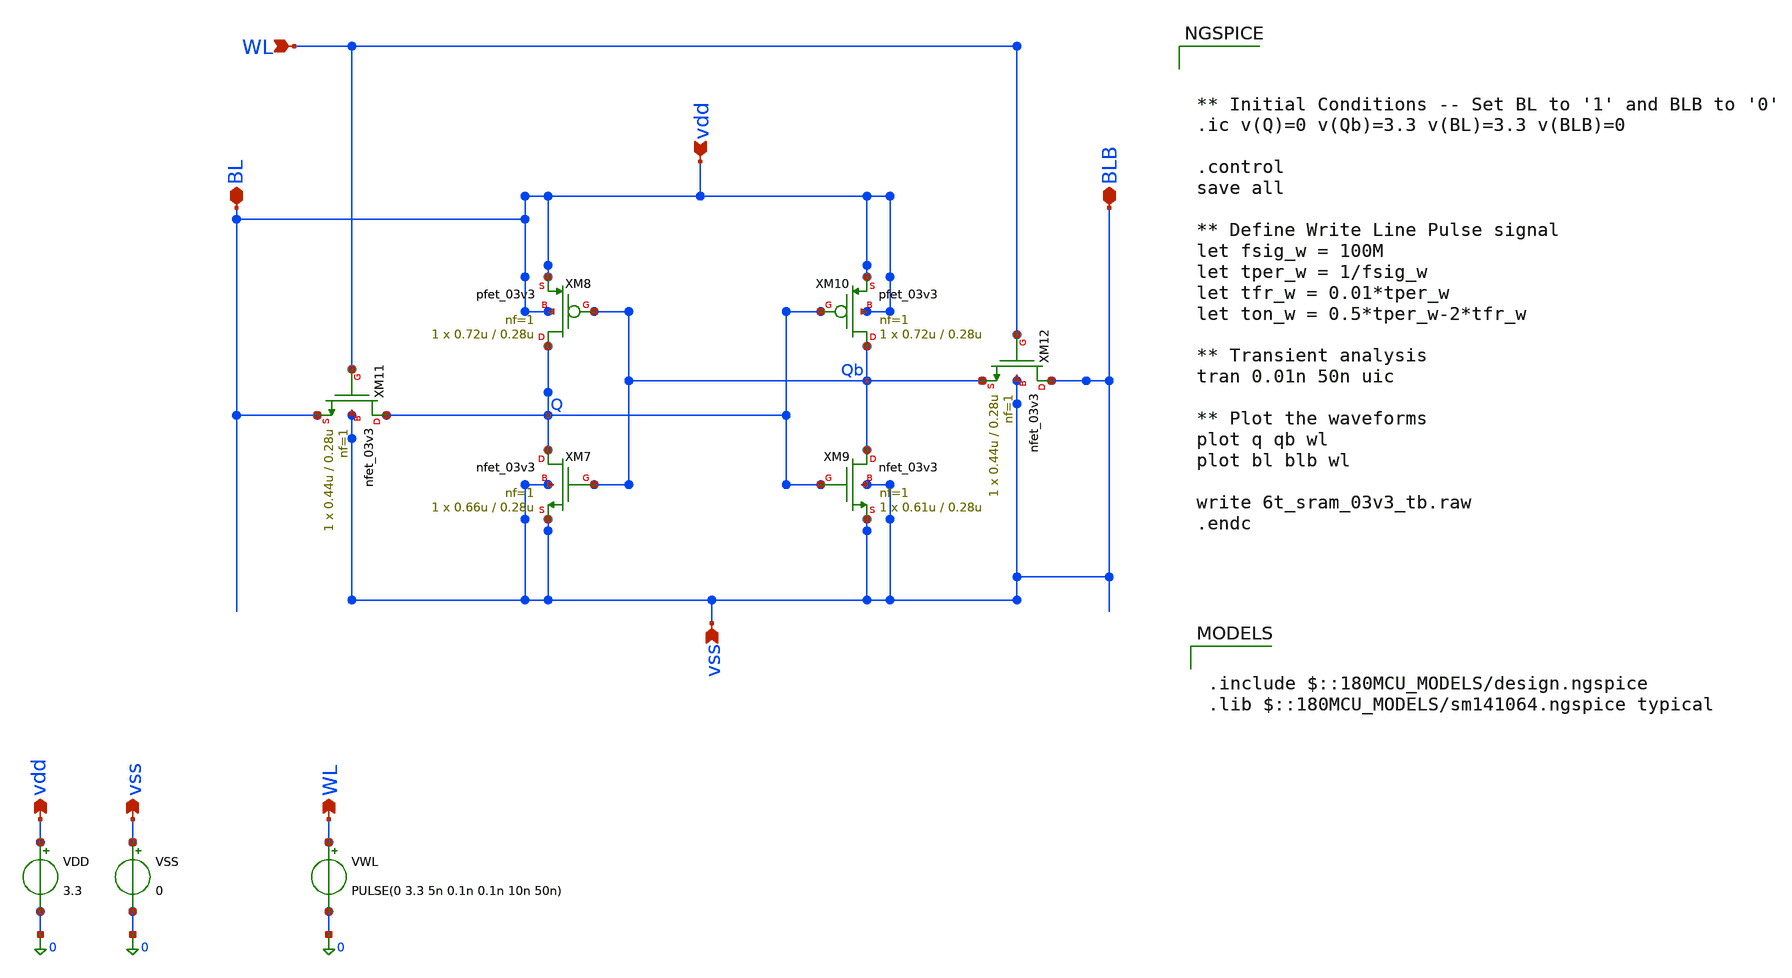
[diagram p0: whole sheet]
** sch_path: analog/designs/6t_sram_03v3_trial.sch
**.subckt 6t_sram_03v3_trial vdd vss WL vdd vss BL WL BLB vdd vss WL vdd vss BL WL BLB
*.opin vdd
*.opin vss
*.opin WL
*.ipin vdd
*.ipin vss
*.iopin BL
*.ipin WL
*.iopin BLB
*.opin vdd
*.opin vss
*.opin WL
*.ipin vdd
*.ipin vss
*.iopin BL
*.ipin WL
*.iopin BLB
VDD vdd 0 3.3
VSS vss 0 0
VWL WL 0 PULSE(0 3.3 5n 0.1n 0.1n 10n 50n)
XM7 Q Qb vss vss nfet_03v3 L=0.28u W=0.66u nf=1 ad='int((nf+1)/2) * W/nf * 0.18u' as='int((nf+2)/2) * W/nf * 0.18u'
+ pd='2*int((nf+1)/2) * (W/nf + 0.18u)' ps='2*int((nf+2)/2) * (W/nf + 0.18u)' nrd='0.18u / W' nrs='0.18u / W'
+ sa=0 sb=0 sd=0 m=1
XM8 Q Qb vdd vdd pfet_03v3 L=0.28u W=0.72u nf=1 ad='int((nf+1)/2) * W/nf * 0.18u' as='int((nf+2)/2) * W/nf * 0.18u'
+ pd='2*int((nf+1)/2) * (W/nf + 0.18u)' ps='2*int((nf+2)/2) * (W/nf + 0.18u)' nrd='0.18u / W' nrs='0.18u / W'
+ sa=0 sb=0 sd=0 m=1
XM9 Qb Q vss vss nfet_03v3 L=0.28u W=0.61u nf=1 ad='int((nf+1)/2) * W/nf * 0.18u' as='int((nf+2)/2) * W/nf * 0.18u'
+ pd='2*int((nf+1)/2) * (W/nf + 0.18u)' ps='2*int((nf+2)/2) * (W/nf + 0.18u)' nrd='0.18u / W' nrs='0.18u / W'
+ sa=0 sb=0 sd=0 m=1
XM10 Qb Q vdd vdd pfet_03v3 L=0.28u W=0.72u nf=1 ad='int((nf+1)/2) * W/nf * 0.18u' as='int((nf+2)/2) * W/nf * 0.18u'
+ pd='2*int((nf+1)/2) * (W/nf + 0.18u)' ps='2*int((nf+2)/2) * (W/nf + 0.18u)' nrd='0.18u / W' nrs='0.18u / W'
+ sa=0 sb=0 sd=0 m=1
XM11 Q WL vdd vss nfet_03v3 L=0.28u W=0.44u nf=1 ad='int((nf+1)/2) * W/nf * 0.18u' as='int((nf+2)/2) * W/nf * 0.18u'
+ pd='2*int((nf+1)/2) * (W/nf + 0.18u)' ps='2*int((nf+2)/2) * (W/nf + 0.18u)' nrd='0.18u / W' nrs='0.18u / W'
+ sa=0 sb=0 sd=0 m=1
XM12 vss WL Qb vss nfet_03v3 L=0.28u W=0.44u nf=1 ad='int((nf+1)/2) * W/nf * 0.18u' as='int((nf+2)/2) * W/nf * 0.18u'
+ pd='2*int((nf+1)/2) * (W/nf + 0.18u)' ps='2*int((nf+2)/2) * (W/nf + 0.18u)' nrd='0.18u / W' nrs='0.18u / W'
+ sa=0 sb=0 sd=0 m=1
VDD vdd 0 3.3
VSS vss 0 0
VWL WL 0 PULSE(0 3.3 5n 0.1n 0.1n 10n 50n)
XM7 Q Qb vss vss nfet_03v3 L=0.28u W=0.66u nf=1 ad='int((nf+1)/2) * W/nf * 0.18u' as='int((nf+2)/2) * W/nf * 0.18u'
+ pd='2*int((nf+1)/2) * (W/nf + 0.18u)' ps='2*int((nf+2)/2) * (W/nf + 0.18u)' nrd='0.18u / W' nrs='0.18u / W'
+ sa=0 sb=0 sd=0 m=1
XM8 Q Qb vdd vdd pfet_03v3 L=0.28u W=0.72u nf=1 ad='int((nf+1)/2) * W/nf * 0.18u' as='int((nf+2)/2) * W/nf * 0.18u'
+ pd='2*int((nf+1)/2) * (W/nf + 0.18u)' ps='2*int((nf+2)/2) * (W/nf + 0.18u)' nrd='0.18u / W' nrs='0.18u / W'
+ sa=0 sb=0 sd=0 m=1
XM9 Qb Q vss vss nfet_03v3 L=0.28u W=0.61u nf=1 ad='int((nf+1)/2) * W/nf * 0.18u' as='int((nf+2)/2) * W/nf * 0.18u'
+ pd='2*int((nf+1)/2) * (W/nf + 0.18u)' ps='2*int((nf+2)/2) * (W/nf + 0.18u)' nrd='0.18u / W' nrs='0.18u / W'
+ sa=0 sb=0 sd=0 m=1
XM10 Qb Q vdd vdd pfet_03v3 L=0.28u W=0.72u nf=1 ad='int((nf+1)/2) * W/nf * 0.18u' as='int((nf+2)/2) * W/nf * 0.18u'
+ pd='2*int((nf+1)/2) * (W/nf + 0.18u)' ps='2*int((nf+2)/2) * (W/nf + 0.18u)' nrd='0.18u / W' nrs='0.18u / W'
+ sa=0 sb=0 sd=0 m=1
XM11 Q WL vdd vss nfet_03v3 L=0.28u W=0.44u nf=1 ad='int((nf+1)/2) * W/nf * 0.18u' as='int((nf+2)/2) * W/nf * 0.18u'
+ pd='2*int((nf+1)/2) * (W/nf + 0.18u)' ps='2*int((nf+2)/2) * (W/nf + 0.18u)' nrd='0.18u / W' nrs='0.18u / W'
+ sa=0 sb=0 sd=0 m=1
XM12 vss WL Qb vss nfet_03v3 L=0.28u W=0.44u nf=1 ad='int((nf+1)/2) * W/nf * 0.18u' as='int((nf+2)/2) * W/nf * 0.18u'
+ pd='2*int((nf+1)/2) * (W/nf + 0.18u)' ps='2*int((nf+2)/2) * (W/nf + 0.18u)' nrd='0.18u / W' nrs='0.18u / W'
+ sa=0 sb=0 sd=0 m=1
**** begin user architecture code

.include $::180MCU_MODELS/design.ngspice
.lib $::180MCU_MODELS/sm141064.ngspice typical




** Initial Conditions -- Set BL to '1' and BLB to '0'
.ic v(Q)=0 v(Qb)=3.3 v(BL)=3.3 v(BLB)=0

.control
save all

** Define Write Line Pulse signal
let fsig_w = 100M
let tper_w = 1/fsig_w
let tfr_w = 0.01*tper_w
let ton_w = 0.5*tper_w-2*tfr_w

** Transient analysis
tran 0.01n 50n uic

** Plot the waveforms
plot q qb wl
plot bl blb wl

write 6t_sram_03v3_tb.raw
.endc




.include $::180MCU_MODELS/design.ngspice
.lib $::180MCU_MODELS/sm141064.ngspice typical




** Initial Conditions -- Set BL to '1' and BLB to '0'
.ic v(Q)=0 v(Qb)=3.3 v(BL)=3.3 v(BLB)=0

.control
save all

** Define Write Line Pulse signal
let fsig_w = 100M
let tper_w = 1/fsig_w
let tfr_w = 0.01*tper_w
let ton_w = 0.5*tper_w-2*tfr_w

** Transient analysis
tran 0.01n 50n uic

** Plot the waveforms
plot q qb wl
plot bl blb wl

write 6t_sram_03v3_tb.raw
.endc



**** end user architecture code
**.ends
.end
